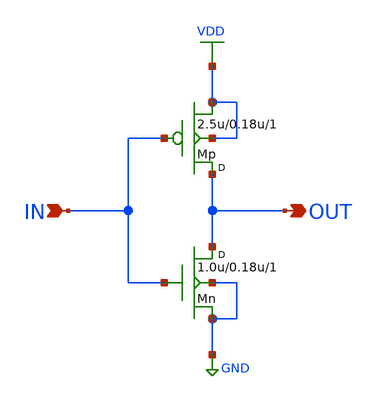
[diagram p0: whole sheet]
** sch_path: E3_238_Analog_VLSI_Circuits/01_CMOS_Inverter/cmos_inverter.sch
**.subckt cmos_inverter IN OUT
*.ipin IN
*.opin OUT
Mp OUT IN VDD VDD pmos w=2.5u l=0.18u m=1
Mn OUT IN GND GND nmos w=1.0u l=0.18u m=1
**** begin user architecture code

.include /home/anirudh/analog_vlsi/models/cmos_180nm.mod
Vdd VDD 0 1.8
Vin IN 0 0 PULSE(0 1.8 1n 50p 50p 5n 10n)
Cload OUT 0 50f

.control
  set color0=white
  set color1=black

  * 1. DC Sweep Analysis & VTC Plot
  dc Vin 0 1.8 0.005
  plot v(OUT) vs v(IN) title '180nm CMOS Inverter DC VTC'

  * 2. Transient Analysis & Switching Plot
  tran 10p 20n
  plot v(IN) v(OUT) title '180nm CMOS Inverter Transient Switching'
.endc


**** end user architecture code
**.ends
.GLOBAL VDD
.GLOBAL GND
.end
